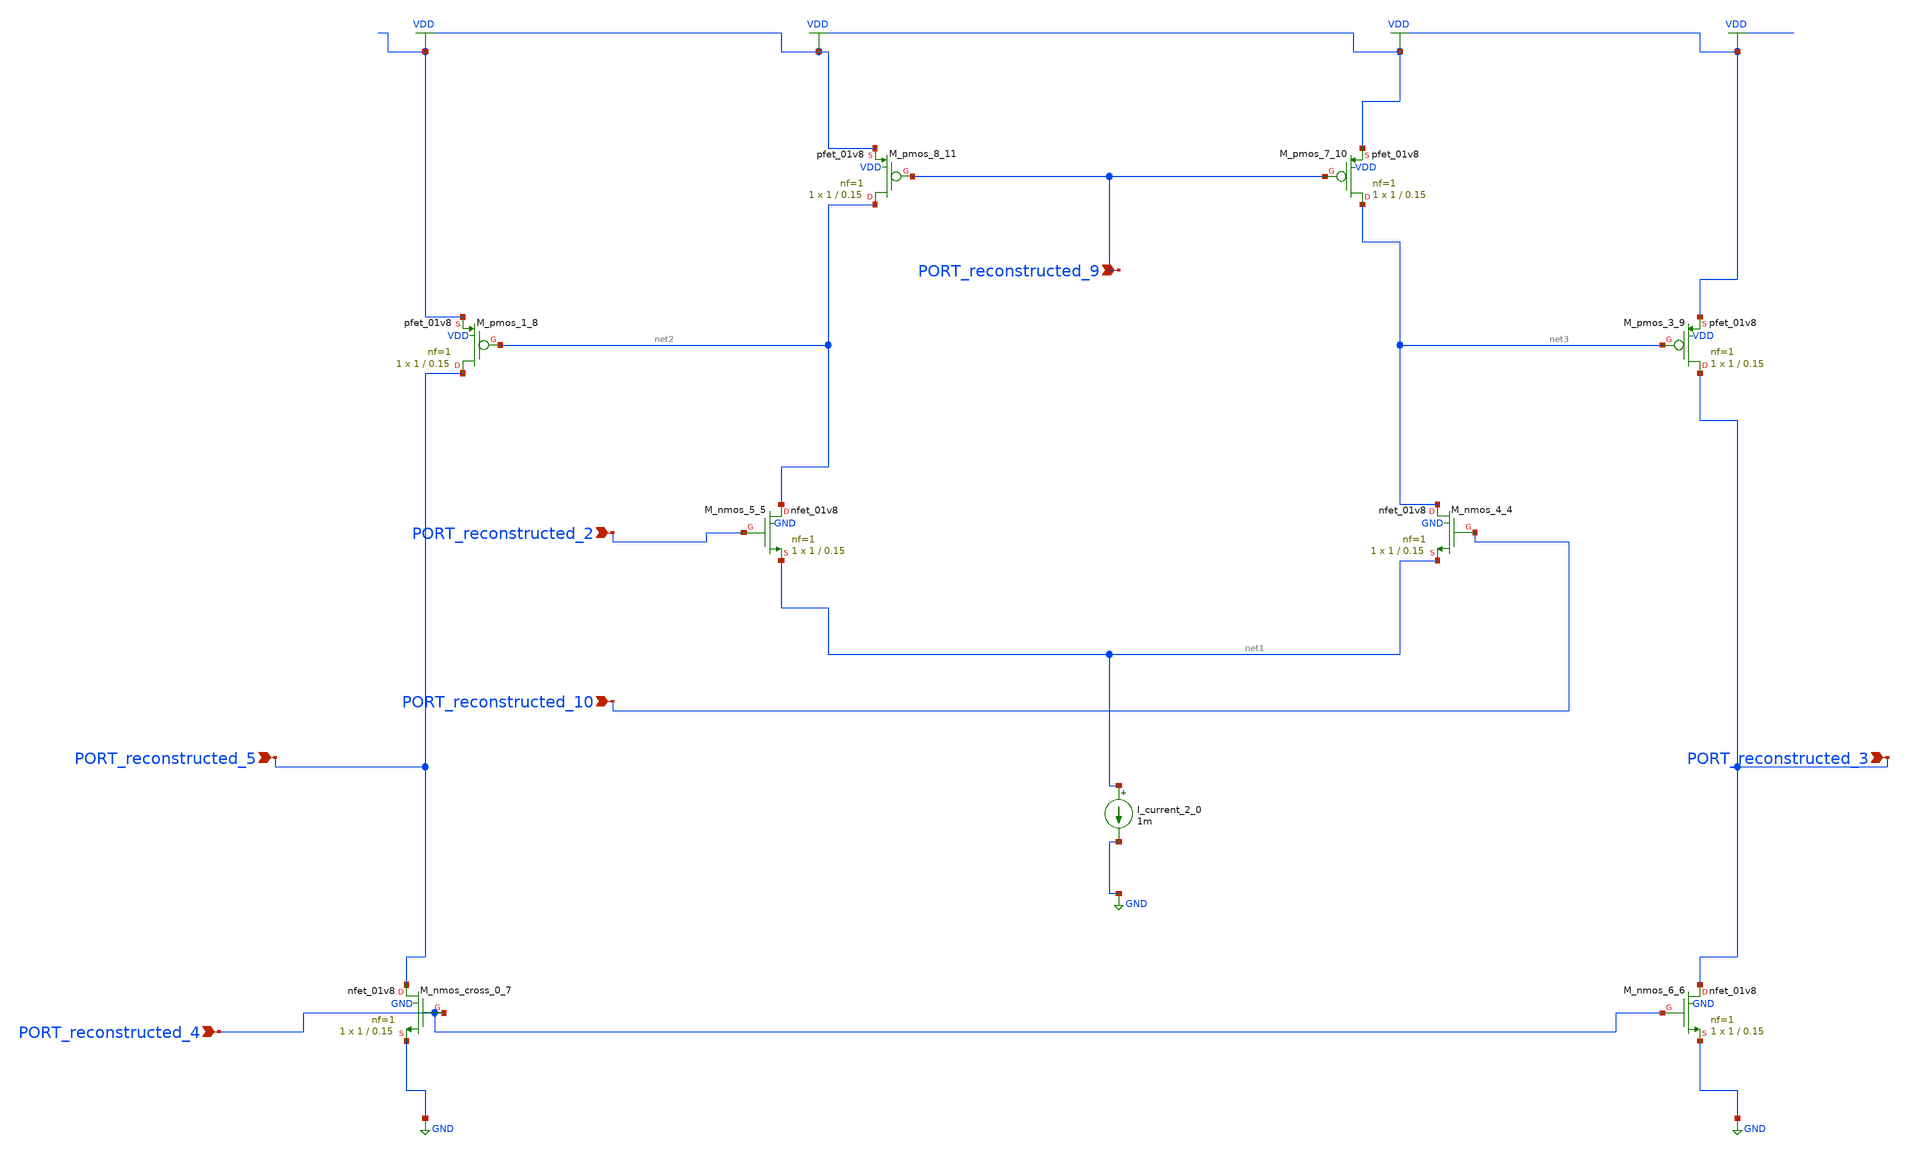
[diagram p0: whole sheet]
** sch_path: schematics/AMSNet/711.sch
**.subckt 711 PORT_reconstructed_10 PORT_reconstructed_5 PORT_reconstructed_2 PORT_reconstructed_3
*+ PORT_reconstructed_4 PORT_reconstructed_9
*.ipin PORT_reconstructed_10
*.ipin PORT_reconstructed_5
*.ipin PORT_reconstructed_2
*.ipin PORT_reconstructed_3
*.ipin PORT_reconstructed_4
*.ipin PORT_reconstructed_9
I_current_2_0 net1 GND 1m
XM_nmos_4_4 net3 PORT_reconstructed_10 net1 GND sky130_fd_pr__nfet_01v8 L=0.15 W=1 nf=1 ad='int((1 + 1)/2) * 1 / 1 * 0.29'
+ as='int((1 + 2)/2) * 1 / 1 * 0.29' pd='2*int((1 + 1)/2) * (1 / 1 + 0.29)' ps='2*int((1 + 2)/2) * (1 / 1 + 0.29)'
+ nrd='0.29 / 1 ' nrs='0.29 / 1 ' sa=0 sb=0 sd=0 mult=1 m=1
XM_nmos_5_5 net2 PORT_reconstructed_2 net1 GND sky130_fd_pr__nfet_01v8 L=0.15 W=1 nf=1 ad='int((1 + 1)/2) * 1 / 1 * 0.29'
+ as='int((1 + 2)/2) * 1 / 1 * 0.29' pd='2*int((1 + 1)/2) * (1 / 1 + 0.29)' ps='2*int((1 + 2)/2) * (1 / 1 + 0.29)'
+ nrd='0.29 / 1 ' nrs='0.29 / 1 ' sa=0 sb=0 sd=0 mult=1 m=1
XM_nmos_6_6 PORT_reconstructed_3 PORT_reconstructed_4 GND GND sky130_fd_pr__nfet_01v8 L=0.15 W=1 nf=1
+ ad='int((1 + 1)/2) * 1 / 1 * 0.29' as='int((1 + 2)/2) * 1 / 1 * 0.29' pd='2*int((1 + 1)/2) * (1 / 1 + 0.29)'
+ ps='2*int((1 + 2)/2) * (1 / 1 + 0.29)' nrd='0.29 / 1 ' nrs='0.29 / 1 ' sa=0 sb=0 sd=0 mult=1 m=1
XM_nmos_cross_0_7 PORT_reconstructed_5 PORT_reconstructed_4 GND GND sky130_fd_pr__nfet_01v8 L=0.15 W=1
+ nf=1 ad='int((1 + 1)/2) * 1 / 1 * 0.29' as='int((1 + 2)/2) * 1 / 1 * 0.29' pd='2*int((1 + 1)/2) * (1 / 1 + 0.29)'
+ ps='2*int((1 + 2)/2) * (1 / 1 + 0.29)' nrd='0.29 / 1 ' nrs='0.29 / 1 ' sa=0 sb=0 sd=0 mult=1 m=1
XM_pmos_1_8 PORT_reconstructed_5 net2 VDD VDD sky130_fd_pr__pfet_01v8 L=0.15 W=1 nf=1 ad='int((1 + 1)/2) * 1 / 1 * 0.29'
+ as='int((1 + 2)/2) * 1 / 1 * 0.29' pd='2*int((1 + 1)/2) * (1 / 1 + 0.29)' ps='2*int((1 + 2)/2) * (1 / 1 + 0.29)'
+ nrd='0.29 / 1 ' nrs='0.29 / 1 ' sa=0 sb=0 sd=0 mult=1 m=1
XM_pmos_3_9 PORT_reconstructed_3 net3 VDD VDD sky130_fd_pr__pfet_01v8 L=0.15 W=1 nf=1 ad='int((1 + 1)/2) * 1 / 1 * 0.29'
+ as='int((1 + 2)/2) * 1 / 1 * 0.29' pd='2*int((1 + 1)/2) * (1 / 1 + 0.29)' ps='2*int((1 + 2)/2) * (1 / 1 + 0.29)'
+ nrd='0.29 / 1 ' nrs='0.29 / 1 ' sa=0 sb=0 sd=0 mult=1 m=1
XM_pmos_7_10 net3 PORT_reconstructed_9 VDD VDD sky130_fd_pr__pfet_01v8 L=0.15 W=1 nf=1 ad='int((1 + 1)/2) * 1 / 1 * 0.29'
+ as='int((1 + 2)/2) * 1 / 1 * 0.29' pd='2*int((1 + 1)/2) * (1 / 1 + 0.29)' ps='2*int((1 + 2)/2) * (1 / 1 + 0.29)'
+ nrd='0.29 / 1 ' nrs='0.29 / 1 ' sa=0 sb=0 sd=0 mult=1 m=1
XM_pmos_8_11 net2 PORT_reconstructed_9 VDD VDD sky130_fd_pr__pfet_01v8 L=0.15 W=1 nf=1 ad='int((1 + 1)/2) * 1 / 1 * 0.29'
+ as='int((1 + 2)/2) * 1 / 1 * 0.29' pd='2*int((1 + 1)/2) * (1 / 1 + 0.29)' ps='2*int((1 + 2)/2) * (1 / 1 + 0.29)'
+ nrd='0.29 / 1 ' nrs='0.29 / 1 ' sa=0 sb=0 sd=0 mult=1 m=1
**.ends
.GLOBAL GND
.GLOBAL VDD
.end
